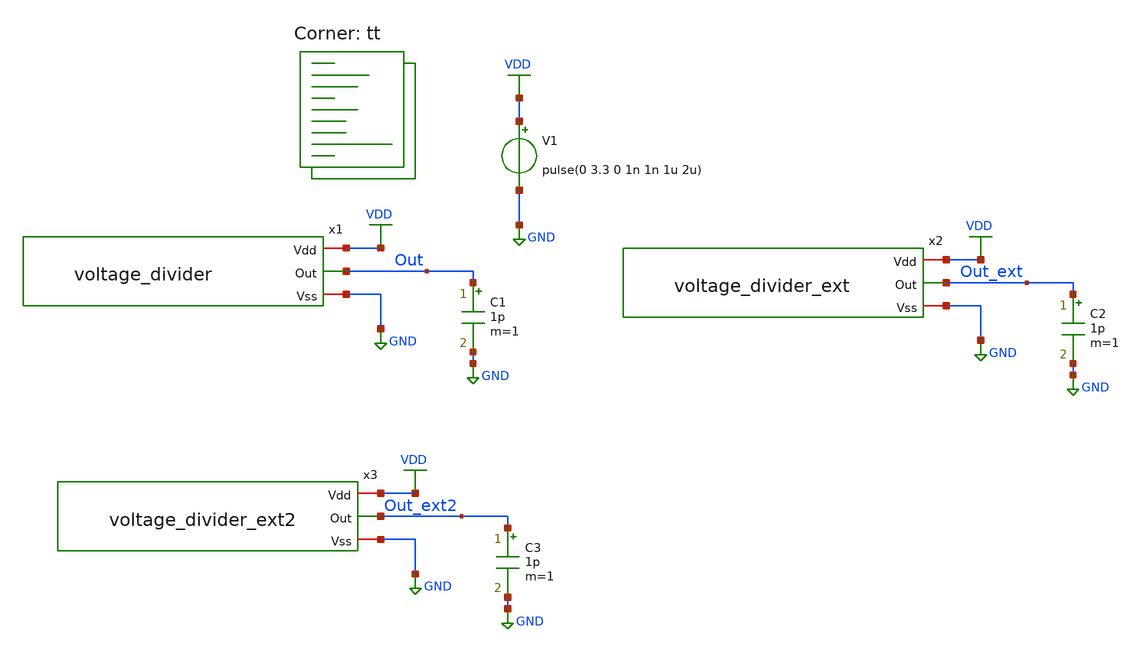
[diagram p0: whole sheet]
** sch_path: xschem/voltage_divider_tb.sch
**.subckt voltage_divider_tb
x1 VDD Out GND voltage_divider
C1 Out GND 1p m=1
V1 VDD GND pulse(0 3.3 0 1n 1n 1u 2u)
x2 VDD Out_ext GND voltage_divider_ext
C2 Out_ext GND 1p m=1
x3 VDD Out_ext2 GND voltage_divider_ext2
C3 Out_ext2 GND 1p m=1
**** begin user architecture code

** opencircuitdesign pdks install
.lib $::SKYWATER_MODELS/sky130.lib.spice tt


.lib $::SKYWATER_MODELS/sky130.lib.spice tt




.control
tran 1n 80u
plot VDD Out Out_ext Out_ext2
save all
.endc



**** end user architecture code
**.ends
.GLOBAL VDD
.GLOBAL GND
.end
